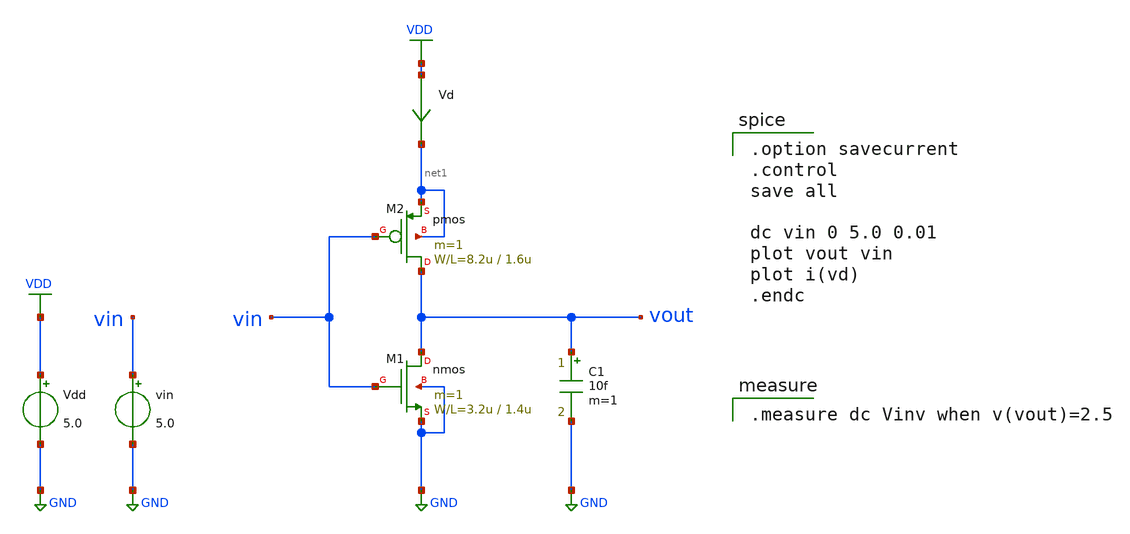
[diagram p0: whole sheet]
** sch_path: member_project/konikoni428/ishi-kai0719-bench.sch
**.subckt ishi-kai0719-bench
vin vin GND 5.0
Vdd VDD GND 5.0
Vd VDD net1 0
.save i(vd)
C1 vout GND 10f m=1
M1 vout vin GND GND nmos L=1.4u W=3.2u m=1
M2 vout vin net1 net1 pmos L=1.6u W=8.2u m=1
**** begin user architecture code

.option savecurrent
.control
save all

dc vin 0 5.0 0.01
plot vout vin
plot i(vd)
.endc


.measure dc Vinv when v(vout)=2.5

 .include $::LIB/mos.lib
.include $::LIB/passive.lib
.include $::LIB/diode.lib
**** end user architecture code
**.ends
.GLOBAL VDD
.GLOBAL GND
.end
